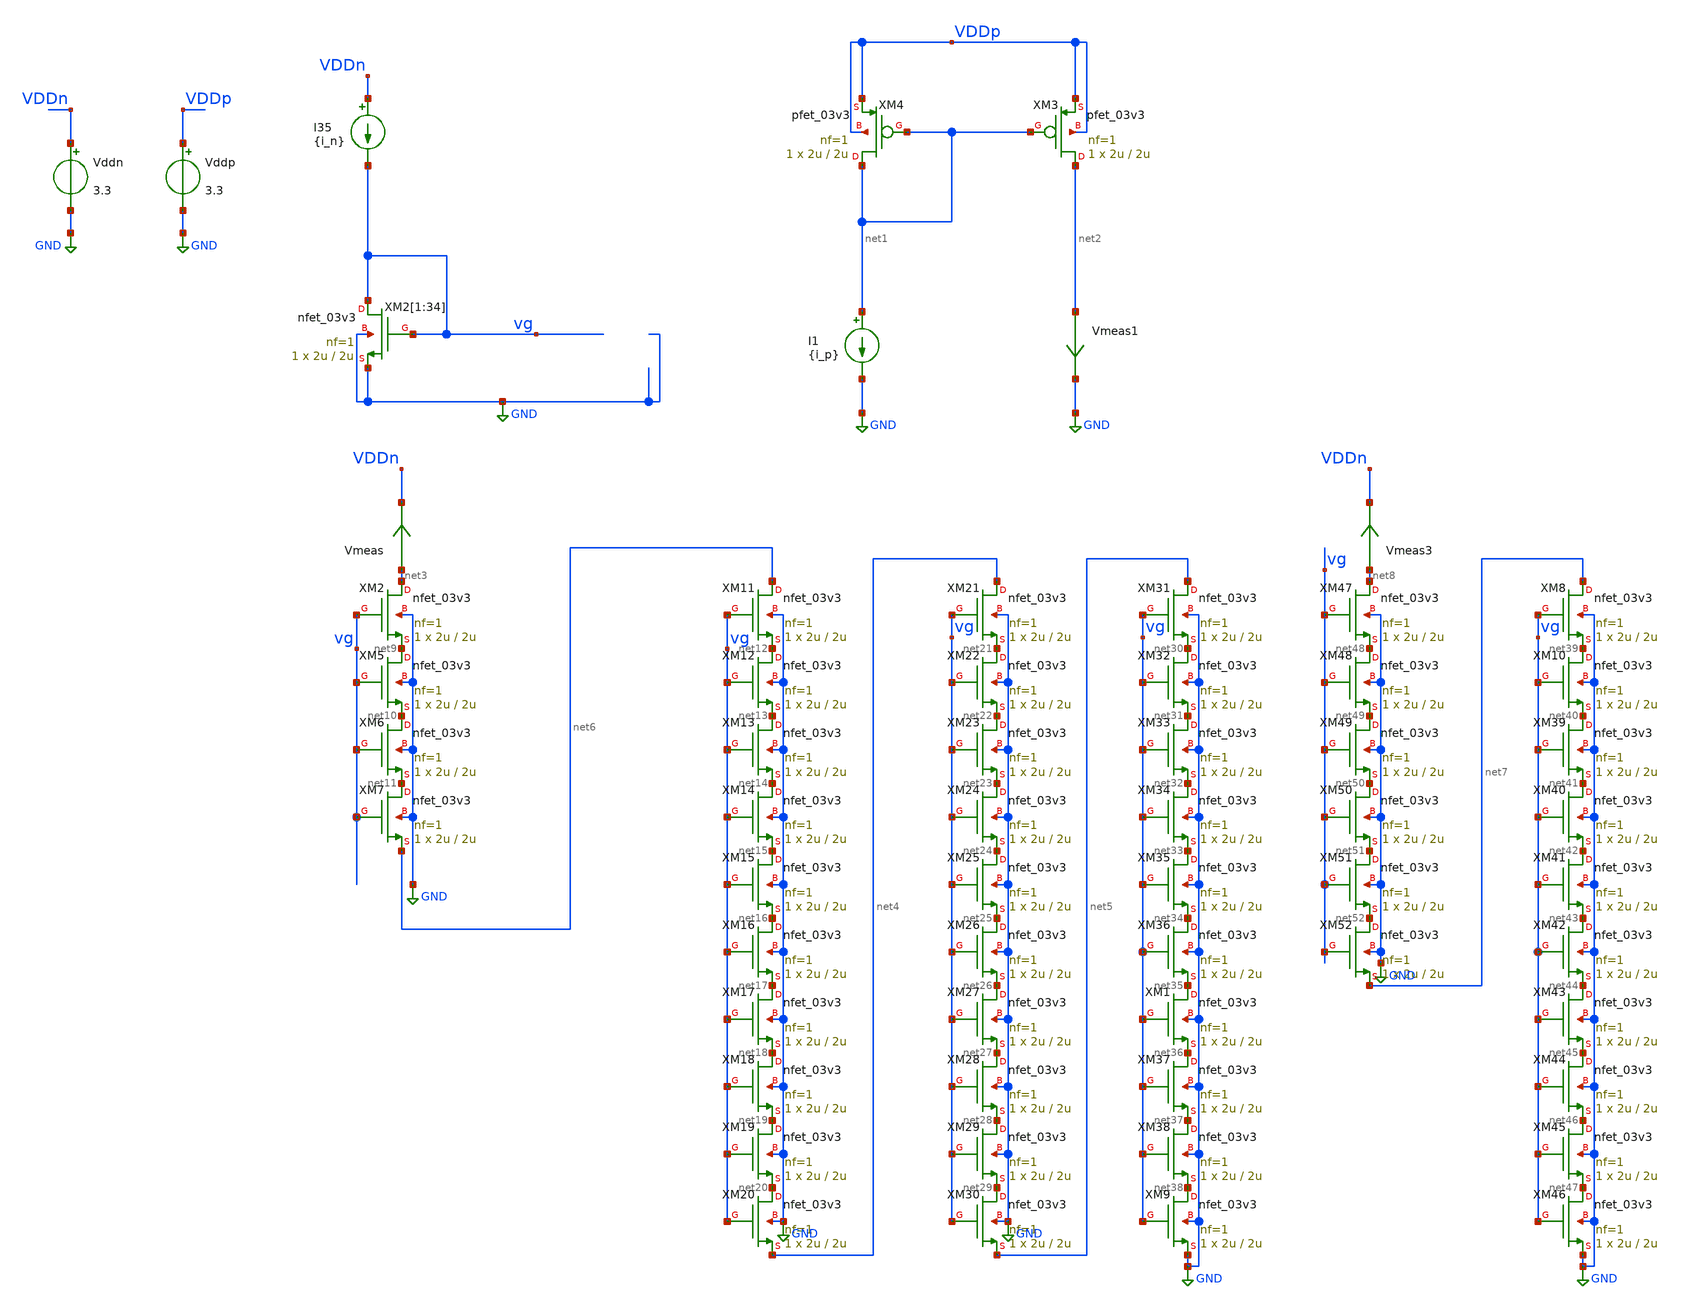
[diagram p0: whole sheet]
** sch_path: TIA_Filter/CurrentMirrors/TB_CM.sch
**.subckt TB_CM
XM2[1] vg vg GND GND nfet_03v3 L=2u W=2u nf=1 ad='int((nf+1)/2) * W/nf * 0.18u' as='int((nf+2)/2) * W/nf * 0.18u'
+ pd='2*int((nf+1)/2) * (W/nf + 0.18u)' ps='2*int((nf+2)/2) * (W/nf + 0.18u)' nrd='0.18u / W' nrs='0.18u / W'
+ sa=0 sb=0 sd=0 m=1
XM2[2] vg vg GND GND nfet_03v3 L=2u W=2u nf=1 ad='int((nf+1)/2) * W/nf * 0.18u' as='int((nf+2)/2) * W/nf * 0.18u'
+ pd='2*int((nf+1)/2) * (W/nf + 0.18u)' ps='2*int((nf+2)/2) * (W/nf + 0.18u)' nrd='0.18u / W' nrs='0.18u / W'
+ sa=0 sb=0 sd=0 m=1
XM2[3] vg vg GND GND nfet_03v3 L=2u W=2u nf=1 ad='int((nf+1)/2) * W/nf * 0.18u' as='int((nf+2)/2) * W/nf * 0.18u'
+ pd='2*int((nf+1)/2) * (W/nf + 0.18u)' ps='2*int((nf+2)/2) * (W/nf + 0.18u)' nrd='0.18u / W' nrs='0.18u / W'
+ sa=0 sb=0 sd=0 m=1
XM2[4] vg vg GND GND nfet_03v3 L=2u W=2u nf=1 ad='int((nf+1)/2) * W/nf * 0.18u' as='int((nf+2)/2) * W/nf * 0.18u'
+ pd='2*int((nf+1)/2) * (W/nf + 0.18u)' ps='2*int((nf+2)/2) * (W/nf + 0.18u)' nrd='0.18u / W' nrs='0.18u / W'
+ sa=0 sb=0 sd=0 m=1
XM2[5] vg vg GND GND nfet_03v3 L=2u W=2u nf=1 ad='int((nf+1)/2) * W/nf * 0.18u' as='int((nf+2)/2) * W/nf * 0.18u'
+ pd='2*int((nf+1)/2) * (W/nf + 0.18u)' ps='2*int((nf+2)/2) * (W/nf + 0.18u)' nrd='0.18u / W' nrs='0.18u / W'
+ sa=0 sb=0 sd=0 m=1
XM2[6] vg vg GND GND nfet_03v3 L=2u W=2u nf=1 ad='int((nf+1)/2) * W/nf * 0.18u' as='int((nf+2)/2) * W/nf * 0.18u'
+ pd='2*int((nf+1)/2) * (W/nf + 0.18u)' ps='2*int((nf+2)/2) * (W/nf + 0.18u)' nrd='0.18u / W' nrs='0.18u / W'
+ sa=0 sb=0 sd=0 m=1
XM2[7] vg vg GND GND nfet_03v3 L=2u W=2u nf=1 ad='int((nf+1)/2) * W/nf * 0.18u' as='int((nf+2)/2) * W/nf * 0.18u'
+ pd='2*int((nf+1)/2) * (W/nf + 0.18u)' ps='2*int((nf+2)/2) * (W/nf + 0.18u)' nrd='0.18u / W' nrs='0.18u / W'
+ sa=0 sb=0 sd=0 m=1
XM2[8] vg vg GND GND nfet_03v3 L=2u W=2u nf=1 ad='int((nf+1)/2) * W/nf * 0.18u' as='int((nf+2)/2) * W/nf * 0.18u'
+ pd='2*int((nf+1)/2) * (W/nf + 0.18u)' ps='2*int((nf+2)/2) * (W/nf + 0.18u)' nrd='0.18u / W' nrs='0.18u / W'
+ sa=0 sb=0 sd=0 m=1
XM2[9] vg vg GND GND nfet_03v3 L=2u W=2u nf=1 ad='int((nf+1)/2) * W/nf * 0.18u' as='int((nf+2)/2) * W/nf * 0.18u'
+ pd='2*int((nf+1)/2) * (W/nf + 0.18u)' ps='2*int((nf+2)/2) * (W/nf + 0.18u)' nrd='0.18u / W' nrs='0.18u / W'
+ sa=0 sb=0 sd=0 m=1
XM2[10] vg vg GND GND nfet_03v3 L=2u W=2u nf=1 ad='int((nf+1)/2) * W/nf * 0.18u' as='int((nf+2)/2) * W/nf * 0.18u'
+ pd='2*int((nf+1)/2) * (W/nf + 0.18u)' ps='2*int((nf+2)/2) * (W/nf + 0.18u)' nrd='0.18u / W' nrs='0.18u / W'
+ sa=0 sb=0 sd=0 m=1
XM2[11] vg vg GND GND nfet_03v3 L=2u W=2u nf=1 ad='int((nf+1)/2) * W/nf * 0.18u' as='int((nf+2)/2) * W/nf * 0.18u'
+ pd='2*int((nf+1)/2) * (W/nf + 0.18u)' ps='2*int((nf+2)/2) * (W/nf + 0.18u)' nrd='0.18u / W' nrs='0.18u / W'
+ sa=0 sb=0 sd=0 m=1
XM2[12] vg vg GND GND nfet_03v3 L=2u W=2u nf=1 ad='int((nf+1)/2) * W/nf * 0.18u' as='int((nf+2)/2) * W/nf * 0.18u'
+ pd='2*int((nf+1)/2) * (W/nf + 0.18u)' ps='2*int((nf+2)/2) * (W/nf + 0.18u)' nrd='0.18u / W' nrs='0.18u / W'
+ sa=0 sb=0 sd=0 m=1
XM2[13] vg vg GND GND nfet_03v3 L=2u W=2u nf=1 ad='int((nf+1)/2) * W/nf * 0.18u' as='int((nf+2)/2) * W/nf * 0.18u'
+ pd='2*int((nf+1)/2) * (W/nf + 0.18u)' ps='2*int((nf+2)/2) * (W/nf + 0.18u)' nrd='0.18u / W' nrs='0.18u / W'
+ sa=0 sb=0 sd=0 m=1
XM2[14] vg vg GND GND nfet_03v3 L=2u W=2u nf=1 ad='int((nf+1)/2) * W/nf * 0.18u' as='int((nf+2)/2) * W/nf * 0.18u'
+ pd='2*int((nf+1)/2) * (W/nf + 0.18u)' ps='2*int((nf+2)/2) * (W/nf + 0.18u)' nrd='0.18u / W' nrs='0.18u / W'
+ sa=0 sb=0 sd=0 m=1
XM2[15] vg vg GND GND nfet_03v3 L=2u W=2u nf=1 ad='int((nf+1)/2) * W/nf * 0.18u' as='int((nf+2)/2) * W/nf * 0.18u'
+ pd='2*int((nf+1)/2) * (W/nf + 0.18u)' ps='2*int((nf+2)/2) * (W/nf + 0.18u)' nrd='0.18u / W' nrs='0.18u / W'
+ sa=0 sb=0 sd=0 m=1
XM2[16] vg vg GND GND nfet_03v3 L=2u W=2u nf=1 ad='int((nf+1)/2) * W/nf * 0.18u' as='int((nf+2)/2) * W/nf * 0.18u'
+ pd='2*int((nf+1)/2) * (W/nf + 0.18u)' ps='2*int((nf+2)/2) * (W/nf + 0.18u)' nrd='0.18u / W' nrs='0.18u / W'
+ sa=0 sb=0 sd=0 m=1
XM2[17] vg vg GND GND nfet_03v3 L=2u W=2u nf=1 ad='int((nf+1)/2) * W/nf * 0.18u' as='int((nf+2)/2) * W/nf * 0.18u'
+ pd='2*int((nf+1)/2) * (W/nf + 0.18u)' ps='2*int((nf+2)/2) * (W/nf + 0.18u)' nrd='0.18u / W' nrs='0.18u / W'
+ sa=0 sb=0 sd=0 m=1
XM2[18] vg vg GND GND nfet_03v3 L=2u W=2u nf=1 ad='int((nf+1)/2) * W/nf * 0.18u' as='int((nf+2)/2) * W/nf * 0.18u'
+ pd='2*int((nf+1)/2) * (W/nf + 0.18u)' ps='2*int((nf+2)/2) * (W/nf + 0.18u)' nrd='0.18u / W' nrs='0.18u / W'
+ sa=0 sb=0 sd=0 m=1
XM2[19] vg vg GND GND nfet_03v3 L=2u W=2u nf=1 ad='int((nf+1)/2) * W/nf * 0.18u' as='int((nf+2)/2) * W/nf * 0.18u'
+ pd='2*int((nf+1)/2) * (W/nf + 0.18u)' ps='2*int((nf+2)/2) * (W/nf + 0.18u)' nrd='0.18u / W' nrs='0.18u / W'
+ sa=0 sb=0 sd=0 m=1
XM2[20] vg vg GND GND nfet_03v3 L=2u W=2u nf=1 ad='int((nf+1)/2) * W/nf * 0.18u' as='int((nf+2)/2) * W/nf * 0.18u'
+ pd='2*int((nf+1)/2) * (W/nf + 0.18u)' ps='2*int((nf+2)/2) * (W/nf + 0.18u)' nrd='0.18u / W' nrs='0.18u / W'
+ sa=0 sb=0 sd=0 m=1
XM2[21] vg vg GND GND nfet_03v3 L=2u W=2u nf=1 ad='int((nf+1)/2) * W/nf * 0.18u' as='int((nf+2)/2) * W/nf * 0.18u'
+ pd='2*int((nf+1)/2) * (W/nf + 0.18u)' ps='2*int((nf+2)/2) * (W/nf + 0.18u)' nrd='0.18u / W' nrs='0.18u / W'
+ sa=0 sb=0 sd=0 m=1
XM2[22] vg vg GND GND nfet_03v3 L=2u W=2u nf=1 ad='int((nf+1)/2) * W/nf * 0.18u' as='int((nf+2)/2) * W/nf * 0.18u'
+ pd='2*int((nf+1)/2) * (W/nf + 0.18u)' ps='2*int((nf+2)/2) * (W/nf + 0.18u)' nrd='0.18u / W' nrs='0.18u / W'
+ sa=0 sb=0 sd=0 m=1
XM2[23] vg vg GND GND nfet_03v3 L=2u W=2u nf=1 ad='int((nf+1)/2) * W/nf * 0.18u' as='int((nf+2)/2) * W/nf * 0.18u'
+ pd='2*int((nf+1)/2) * (W/nf + 0.18u)' ps='2*int((nf+2)/2) * (W/nf + 0.18u)' nrd='0.18u / W' nrs='0.18u / W'
+ sa=0 sb=0 sd=0 m=1
XM2[24] vg vg GND GND nfet_03v3 L=2u W=2u nf=1 ad='int((nf+1)/2) * W/nf * 0.18u' as='int((nf+2)/2) * W/nf * 0.18u'
+ pd='2*int((nf+1)/2) * (W/nf + 0.18u)' ps='2*int((nf+2)/2) * (W/nf + 0.18u)' nrd='0.18u / W' nrs='0.18u / W'
+ sa=0 sb=0 sd=0 m=1
XM2[25] vg vg GND GND nfet_03v3 L=2u W=2u nf=1 ad='int((nf+1)/2) * W/nf * 0.18u' as='int((nf+2)/2) * W/nf * 0.18u'
+ pd='2*int((nf+1)/2) * (W/nf + 0.18u)' ps='2*int((nf+2)/2) * (W/nf + 0.18u)' nrd='0.18u / W' nrs='0.18u / W'
+ sa=0 sb=0 sd=0 m=1
XM2[26] vg vg GND GND nfet_03v3 L=2u W=2u nf=1 ad='int((nf+1)/2) * W/nf * 0.18u' as='int((nf+2)/2) * W/nf * 0.18u'
+ pd='2*int((nf+1)/2) * (W/nf + 0.18u)' ps='2*int((nf+2)/2) * (W/nf + 0.18u)' nrd='0.18u / W' nrs='0.18u / W'
+ sa=0 sb=0 sd=0 m=1
XM2[27] vg vg GND GND nfet_03v3 L=2u W=2u nf=1 ad='int((nf+1)/2) * W/nf * 0.18u' as='int((nf+2)/2) * W/nf * 0.18u'
+ pd='2*int((nf+1)/2) * (W/nf + 0.18u)' ps='2*int((nf+2)/2) * (W/nf + 0.18u)' nrd='0.18u / W' nrs='0.18u / W'
+ sa=0 sb=0 sd=0 m=1
XM2[28] vg vg GND GND nfet_03v3 L=2u W=2u nf=1 ad='int((nf+1)/2) * W/nf * 0.18u' as='int((nf+2)/2) * W/nf * 0.18u'
+ pd='2*int((nf+1)/2) * (W/nf + 0.18u)' ps='2*int((nf+2)/2) * (W/nf + 0.18u)' nrd='0.18u / W' nrs='0.18u / W'
+ sa=0 sb=0 sd=0 m=1
XM2[29] vg vg GND GND nfet_03v3 L=2u W=2u nf=1 ad='int((nf+1)/2) * W/nf * 0.18u' as='int((nf+2)/2) * W/nf * 0.18u'
+ pd='2*int((nf+1)/2) * (W/nf + 0.18u)' ps='2*int((nf+2)/2) * (W/nf + 0.18u)' nrd='0.18u / W' nrs='0.18u / W'
+ sa=0 sb=0 sd=0 m=1
XM2[30] vg vg GND GND nfet_03v3 L=2u W=2u nf=1 ad='int((nf+1)/2) * W/nf * 0.18u' as='int((nf+2)/2) * W/nf * 0.18u'
+ pd='2*int((nf+1)/2) * (W/nf + 0.18u)' ps='2*int((nf+2)/2) * (W/nf + 0.18u)' nrd='0.18u / W' nrs='0.18u / W'
+ sa=0 sb=0 sd=0 m=1
XM2[31] vg vg GND GND nfet_03v3 L=2u W=2u nf=1 ad='int((nf+1)/2) * W/nf * 0.18u' as='int((nf+2)/2) * W/nf * 0.18u'
+ pd='2*int((nf+1)/2) * (W/nf + 0.18u)' ps='2*int((nf+2)/2) * (W/nf + 0.18u)' nrd='0.18u / W' nrs='0.18u / W'
+ sa=0 sb=0 sd=0 m=1
XM2[32] vg vg GND GND nfet_03v3 L=2u W=2u nf=1 ad='int((nf+1)/2) * W/nf * 0.18u' as='int((nf+2)/2) * W/nf * 0.18u'
+ pd='2*int((nf+1)/2) * (W/nf + 0.18u)' ps='2*int((nf+2)/2) * (W/nf + 0.18u)' nrd='0.18u / W' nrs='0.18u / W'
+ sa=0 sb=0 sd=0 m=1
XM2[33] vg vg GND GND nfet_03v3 L=2u W=2u nf=1 ad='int((nf+1)/2) * W/nf * 0.18u' as='int((nf+2)/2) * W/nf * 0.18u'
+ pd='2*int((nf+1)/2) * (W/nf + 0.18u)' ps='2*int((nf+2)/2) * (W/nf + 0.18u)' nrd='0.18u / W' nrs='0.18u / W'
+ sa=0 sb=0 sd=0 m=1
XM2[34] vg vg GND GND nfet_03v3 L=2u W=2u nf=1 ad='int((nf+1)/2) * W/nf * 0.18u' as='int((nf+2)/2) * W/nf * 0.18u'
+ pd='2*int((nf+1)/2) * (W/nf + 0.18u)' ps='2*int((nf+2)/2) * (W/nf + 0.18u)' nrd='0.18u / W' nrs='0.18u / W'
+ sa=0 sb=0 sd=0 m=1
XM3 net2 net1 VDDp VDDp pfet_03v3 L=2u W=2u nf=1 ad='int((nf+1)/2) * W/nf * 0.18u' as='int((nf+2)/2) * W/nf * 0.18u'
+ pd='2*int((nf+1)/2) * (W/nf + 0.18u)' ps='2*int((nf+2)/2) * (W/nf + 0.18u)' nrd='0.18u / W' nrs='0.18u / W'
+ sa=0 sb=0 sd=0 m=1
XM4 net1 net1 VDDp VDDp pfet_03v3 L=2u W=2u nf=1 ad='int((nf+1)/2) * W/nf * 0.18u' as='int((nf+2)/2) * W/nf * 0.18u'
+ pd='2*int((nf+1)/2) * (W/nf + 0.18u)' ps='2*int((nf+2)/2) * (W/nf + 0.18u)' nrd='0.18u / W' nrs='0.18u / W'
+ sa=0 sb=0 sd=0 m=1
I35 VDDn vg {i_n}
I1 net1 GND {i_p}
Vddn VDDn GND 3.3
Vddp VDDp GND 3.3
Vmeas net3 VDDn 0
.save i(vmeas)
Vmeas1 net2 GND 0
.save i(vmeas1)
XM2 net3 vg net9 GND nfet_03v3 L=2u W=2u nf=1 ad='int((nf+1)/2) * W/nf * 0.18u' as='int((nf+2)/2) * W/nf * 0.18u'
+ pd='2*int((nf+1)/2) * (W/nf + 0.18u)' ps='2*int((nf+2)/2) * (W/nf + 0.18u)' nrd='0.18u / W' nrs='0.18u / W'
+ sa=0 sb=0 sd=0 m=1
XM5 net9 vg net10 GND nfet_03v3 L=2u W=2u nf=1 ad='int((nf+1)/2) * W/nf * 0.18u' as='int((nf+2)/2) * W/nf * 0.18u'
+ pd='2*int((nf+1)/2) * (W/nf + 0.18u)' ps='2*int((nf+2)/2) * (W/nf + 0.18u)' nrd='0.18u / W' nrs='0.18u / W'
+ sa=0 sb=0 sd=0 m=1
XM6 net10 vg net11 GND nfet_03v3 L=2u W=2u nf=1 ad='int((nf+1)/2) * W/nf * 0.18u' as='int((nf+2)/2) * W/nf * 0.18u'
+ pd='2*int((nf+1)/2) * (W/nf + 0.18u)' ps='2*int((nf+2)/2) * (W/nf + 0.18u)' nrd='0.18u / W' nrs='0.18u / W'
+ sa=0 sb=0 sd=0 m=1
XM7 net11 vg net6 GND nfet_03v3 L=2u W=2u nf=1 ad='int((nf+1)/2) * W/nf * 0.18u' as='int((nf+2)/2) * W/nf * 0.18u'
+ pd='2*int((nf+1)/2) * (W/nf + 0.18u)' ps='2*int((nf+2)/2) * (W/nf + 0.18u)' nrd='0.18u / W' nrs='0.18u / W'
+ sa=0 sb=0 sd=0 m=1
XM11 net6 vg net12 GND nfet_03v3 L=2u W=2u nf=1 ad='int((nf+1)/2) * W/nf * 0.18u' as='int((nf+2)/2) * W/nf * 0.18u'
+ pd='2*int((nf+1)/2) * (W/nf + 0.18u)' ps='2*int((nf+2)/2) * (W/nf + 0.18u)' nrd='0.18u / W' nrs='0.18u / W'
+ sa=0 sb=0 sd=0 m=1
XM12 net12 vg net13 GND nfet_03v3 L=2u W=2u nf=1 ad='int((nf+1)/2) * W/nf * 0.18u' as='int((nf+2)/2) * W/nf * 0.18u'
+ pd='2*int((nf+1)/2) * (W/nf + 0.18u)' ps='2*int((nf+2)/2) * (W/nf + 0.18u)' nrd='0.18u / W' nrs='0.18u / W'
+ sa=0 sb=0 sd=0 m=1
XM13 net13 vg net14 GND nfet_03v3 L=2u W=2u nf=1 ad='int((nf+1)/2) * W/nf * 0.18u' as='int((nf+2)/2) * W/nf * 0.18u'
+ pd='2*int((nf+1)/2) * (W/nf + 0.18u)' ps='2*int((nf+2)/2) * (W/nf + 0.18u)' nrd='0.18u / W' nrs='0.18u / W'
+ sa=0 sb=0 sd=0 m=1
XM14 net14 vg net15 GND nfet_03v3 L=2u W=2u nf=1 ad='int((nf+1)/2) * W/nf * 0.18u' as='int((nf+2)/2) * W/nf * 0.18u'
+ pd='2*int((nf+1)/2) * (W/nf + 0.18u)' ps='2*int((nf+2)/2) * (W/nf + 0.18u)' nrd='0.18u / W' nrs='0.18u / W'
+ sa=0 sb=0 sd=0 m=1
XM15 net15 vg net16 GND nfet_03v3 L=2u W=2u nf=1 ad='int((nf+1)/2) * W/nf * 0.18u' as='int((nf+2)/2) * W/nf * 0.18u'
+ pd='2*int((nf+1)/2) * (W/nf + 0.18u)' ps='2*int((nf+2)/2) * (W/nf + 0.18u)' nrd='0.18u / W' nrs='0.18u / W'
+ sa=0 sb=0 sd=0 m=1
XM16 net16 vg net17 GND nfet_03v3 L=2u W=2u nf=1 ad='int((nf+1)/2) * W/nf * 0.18u' as='int((nf+2)/2) * W/nf * 0.18u'
+ pd='2*int((nf+1)/2) * (W/nf + 0.18u)' ps='2*int((nf+2)/2) * (W/nf + 0.18u)' nrd='0.18u / W' nrs='0.18u / W'
+ sa=0 sb=0 sd=0 m=1
XM17 net17 vg net18 GND nfet_03v3 L=2u W=2u nf=1 ad='int((nf+1)/2) * W/nf * 0.18u' as='int((nf+2)/2) * W/nf * 0.18u'
+ pd='2*int((nf+1)/2) * (W/nf + 0.18u)' ps='2*int((nf+2)/2) * (W/nf + 0.18u)' nrd='0.18u / W' nrs='0.18u / W'
+ sa=0 sb=0 sd=0 m=1
XM18 net18 vg net19 GND nfet_03v3 L=2u W=2u nf=1 ad='int((nf+1)/2) * W/nf * 0.18u' as='int((nf+2)/2) * W/nf * 0.18u'
+ pd='2*int((nf+1)/2) * (W/nf + 0.18u)' ps='2*int((nf+2)/2) * (W/nf + 0.18u)' nrd='0.18u / W' nrs='0.18u / W'
+ sa=0 sb=0 sd=0 m=1
XM19 net19 vg net20 GND nfet_03v3 L=2u W=2u nf=1 ad='int((nf+1)/2) * W/nf * 0.18u' as='int((nf+2)/2) * W/nf * 0.18u'
+ pd='2*int((nf+1)/2) * (W/nf + 0.18u)' ps='2*int((nf+2)/2) * (W/nf + 0.18u)' nrd='0.18u / W' nrs='0.18u / W'
+ sa=0 sb=0 sd=0 m=1
XM20 net20 vg net4 GND nfet_03v3 L=2u W=2u nf=1 ad='int((nf+1)/2) * W/nf * 0.18u' as='int((nf+2)/2) * W/nf * 0.18u'
+ pd='2*int((nf+1)/2) * (W/nf + 0.18u)' ps='2*int((nf+2)/2) * (W/nf + 0.18u)' nrd='0.18u / W' nrs='0.18u / W'
+ sa=0 sb=0 sd=0 m=1
XM21 net4 vg net21 GND nfet_03v3 L=2u W=2u nf=1 ad='int((nf+1)/2) * W/nf * 0.18u' as='int((nf+2)/2) * W/nf * 0.18u'
+ pd='2*int((nf+1)/2) * (W/nf + 0.18u)' ps='2*int((nf+2)/2) * (W/nf + 0.18u)' nrd='0.18u / W' nrs='0.18u / W'
+ sa=0 sb=0 sd=0 m=1
XM22 net21 vg net22 GND nfet_03v3 L=2u W=2u nf=1 ad='int((nf+1)/2) * W/nf * 0.18u' as='int((nf+2)/2) * W/nf * 0.18u'
+ pd='2*int((nf+1)/2) * (W/nf + 0.18u)' ps='2*int((nf+2)/2) * (W/nf + 0.18u)' nrd='0.18u / W' nrs='0.18u / W'
+ sa=0 sb=0 sd=0 m=1
XM23 net22 vg net23 GND nfet_03v3 L=2u W=2u nf=1 ad='int((nf+1)/2) * W/nf * 0.18u' as='int((nf+2)/2) * W/nf * 0.18u'
+ pd='2*int((nf+1)/2) * (W/nf + 0.18u)' ps='2*int((nf+2)/2) * (W/nf + 0.18u)' nrd='0.18u / W' nrs='0.18u / W'
+ sa=0 sb=0 sd=0 m=1
XM24 net23 vg net24 GND nfet_03v3 L=2u W=2u nf=1 ad='int((nf+1)/2) * W/nf * 0.18u' as='int((nf+2)/2) * W/nf * 0.18u'
+ pd='2*int((nf+1)/2) * (W/nf + 0.18u)' ps='2*int((nf+2)/2) * (W/nf + 0.18u)' nrd='0.18u / W' nrs='0.18u / W'
+ sa=0 sb=0 sd=0 m=1
XM25 net24 vg net25 GND nfet_03v3 L=2u W=2u nf=1 ad='int((nf+1)/2) * W/nf * 0.18u' as='int((nf+2)/2) * W/nf * 0.18u'
+ pd='2*int((nf+1)/2) * (W/nf + 0.18u)' ps='2*int((nf+2)/2) * (W/nf + 0.18u)' nrd='0.18u / W' nrs='0.18u / W'
+ sa=0 sb=0 sd=0 m=1
XM26 net25 vg net26 GND nfet_03v3 L=2u W=2u nf=1 ad='int((nf+1)/2) * W/nf * 0.18u' as='int((nf+2)/2) * W/nf * 0.18u'
+ pd='2*int((nf+1)/2) * (W/nf + 0.18u)' ps='2*int((nf+2)/2) * (W/nf + 0.18u)' nrd='0.18u / W' nrs='0.18u / W'
+ sa=0 sb=0 sd=0 m=1
XM27 net26 vg net27 GND nfet_03v3 L=2u W=2u nf=1 ad='int((nf+1)/2) * W/nf * 0.18u' as='int((nf+2)/2) * W/nf * 0.18u'
+ pd='2*int((nf+1)/2) * (W/nf + 0.18u)' ps='2*int((nf+2)/2) * (W/nf + 0.18u)' nrd='0.18u / W' nrs='0.18u / W'
+ sa=0 sb=0 sd=0 m=1
XM28 net27 vg net28 GND nfet_03v3 L=2u W=2u nf=1 ad='int((nf+1)/2) * W/nf * 0.18u' as='int((nf+2)/2) * W/nf * 0.18u'
+ pd='2*int((nf+1)/2) * (W/nf + 0.18u)' ps='2*int((nf+2)/2) * (W/nf + 0.18u)' nrd='0.18u / W' nrs='0.18u / W'
+ sa=0 sb=0 sd=0 m=1
XM29 net28 vg net29 GND nfet_03v3 L=2u W=2u nf=1 ad='int((nf+1)/2) * W/nf * 0.18u' as='int((nf+2)/2) * W/nf * 0.18u'
+ pd='2*int((nf+1)/2) * (W/nf + 0.18u)' ps='2*int((nf+2)/2) * (W/nf + 0.18u)' nrd='0.18u / W' nrs='0.18u / W'
+ sa=0 sb=0 sd=0 m=1
XM30 net29 vg net5 GND nfet_03v3 L=2u W=2u nf=1 ad='int((nf+1)/2) * W/nf * 0.18u' as='int((nf+2)/2) * W/nf * 0.18u'
+ pd='2*int((nf+1)/2) * (W/nf + 0.18u)' ps='2*int((nf+2)/2) * (W/nf + 0.18u)' nrd='0.18u / W' nrs='0.18u / W'
+ sa=0 sb=0 sd=0 m=1
XM31 net5 vg net30 GND nfet_03v3 L=2u W=2u nf=1 ad='int((nf+1)/2) * W/nf * 0.18u' as='int((nf+2)/2) * W/nf * 0.18u'
+ pd='2*int((nf+1)/2) * (W/nf + 0.18u)' ps='2*int((nf+2)/2) * (W/nf + 0.18u)' nrd='0.18u / W' nrs='0.18u / W'
+ sa=0 sb=0 sd=0 m=1
XM32 net30 vg net31 GND nfet_03v3 L=2u W=2u nf=1 ad='int((nf+1)/2) * W/nf * 0.18u' as='int((nf+2)/2) * W/nf * 0.18u'
+ pd='2*int((nf+1)/2) * (W/nf + 0.18u)' ps='2*int((nf+2)/2) * (W/nf + 0.18u)' nrd='0.18u / W' nrs='0.18u / W'
+ sa=0 sb=0 sd=0 m=1
XM33 net31 vg net32 GND nfet_03v3 L=2u W=2u nf=1 ad='int((nf+1)/2) * W/nf * 0.18u' as='int((nf+2)/2) * W/nf * 0.18u'
+ pd='2*int((nf+1)/2) * (W/nf + 0.18u)' ps='2*int((nf+2)/2) * (W/nf + 0.18u)' nrd='0.18u / W' nrs='0.18u / W'
+ sa=0 sb=0 sd=0 m=1
XM34 net32 vg net33 GND nfet_03v3 L=2u W=2u nf=1 ad='int((nf+1)/2) * W/nf * 0.18u' as='int((nf+2)/2) * W/nf * 0.18u'
+ pd='2*int((nf+1)/2) * (W/nf + 0.18u)' ps='2*int((nf+2)/2) * (W/nf + 0.18u)' nrd='0.18u / W' nrs='0.18u / W'
+ sa=0 sb=0 sd=0 m=1
XM35 net33 vg net34 GND nfet_03v3 L=2u W=2u nf=1 ad='int((nf+1)/2) * W/nf * 0.18u' as='int((nf+2)/2) * W/nf * 0.18u'
+ pd='2*int((nf+1)/2) * (W/nf + 0.18u)' ps='2*int((nf+2)/2) * (W/nf + 0.18u)' nrd='0.18u / W' nrs='0.18u / W'
+ sa=0 sb=0 sd=0 m=1
XM36 net34 vg net35 GND nfet_03v3 L=2u W=2u nf=1 ad='int((nf+1)/2) * W/nf * 0.18u' as='int((nf+2)/2) * W/nf * 0.18u'
+ pd='2*int((nf+1)/2) * (W/nf + 0.18u)' ps='2*int((nf+2)/2) * (W/nf + 0.18u)' nrd='0.18u / W' nrs='0.18u / W'
+ sa=0 sb=0 sd=0 m=1
XM1 net35 vg net36 GND nfet_03v3 L=2u W=2u nf=1 ad='int((nf+1)/2) * W/nf * 0.18u' as='int((nf+2)/2) * W/nf * 0.18u'
+ pd='2*int((nf+1)/2) * (W/nf + 0.18u)' ps='2*int((nf+2)/2) * (W/nf + 0.18u)' nrd='0.18u / W' nrs='0.18u / W'
+ sa=0 sb=0 sd=0 m=1
XM37 net36 vg net37 GND nfet_03v3 L=2u W=2u nf=1 ad='int((nf+1)/2) * W/nf * 0.18u' as='int((nf+2)/2) * W/nf * 0.18u'
+ pd='2*int((nf+1)/2) * (W/nf + 0.18u)' ps='2*int((nf+2)/2) * (W/nf + 0.18u)' nrd='0.18u / W' nrs='0.18u / W'
+ sa=0 sb=0 sd=0 m=1
XM38 net37 vg net38 GND nfet_03v3 L=2u W=2u nf=1 ad='int((nf+1)/2) * W/nf * 0.18u' as='int((nf+2)/2) * W/nf * 0.18u'
+ pd='2*int((nf+1)/2) * (W/nf + 0.18u)' ps='2*int((nf+2)/2) * (W/nf + 0.18u)' nrd='0.18u / W' nrs='0.18u / W'
+ sa=0 sb=0 sd=0 m=1
XM9 net38 vg GND GND nfet_03v3 L=2u W=2u nf=1 ad='int((nf+1)/2) * W/nf * 0.18u' as='int((nf+2)/2) * W/nf * 0.18u'
+ pd='2*int((nf+1)/2) * (W/nf + 0.18u)' ps='2*int((nf+2)/2) * (W/nf + 0.18u)' nrd='0.18u / W' nrs='0.18u / W'
+ sa=0 sb=0 sd=0 m=1
XM8 net7 vg net39 GND nfet_03v3 L=2u W=2u nf=1 ad='int((nf+1)/2) * W/nf * 0.18u' as='int((nf+2)/2) * W/nf * 0.18u'
+ pd='2*int((nf+1)/2) * (W/nf + 0.18u)' ps='2*int((nf+2)/2) * (W/nf + 0.18u)' nrd='0.18u / W' nrs='0.18u / W'
+ sa=0 sb=0 sd=0 m=1
XM10 net39 vg net40 GND nfet_03v3 L=2u W=2u nf=1 ad='int((nf+1)/2) * W/nf * 0.18u' as='int((nf+2)/2) * W/nf * 0.18u'
+ pd='2*int((nf+1)/2) * (W/nf + 0.18u)' ps='2*int((nf+2)/2) * (W/nf + 0.18u)' nrd='0.18u / W' nrs='0.18u / W'
+ sa=0 sb=0 sd=0 m=1
XM39 net40 vg net41 GND nfet_03v3 L=2u W=2u nf=1 ad='int((nf+1)/2) * W/nf * 0.18u' as='int((nf+2)/2) * W/nf * 0.18u'
+ pd='2*int((nf+1)/2) * (W/nf + 0.18u)' ps='2*int((nf+2)/2) * (W/nf + 0.18u)' nrd='0.18u / W' nrs='0.18u / W'
+ sa=0 sb=0 sd=0 m=1
XM40 net41 vg net42 GND nfet_03v3 L=2u W=2u nf=1 ad='int((nf+1)/2) * W/nf * 0.18u' as='int((nf+2)/2) * W/nf * 0.18u'
+ pd='2*int((nf+1)/2) * (W/nf + 0.18u)' ps='2*int((nf+2)/2) * (W/nf + 0.18u)' nrd='0.18u / W' nrs='0.18u / W'
+ sa=0 sb=0 sd=0 m=1
XM41 net42 vg net43 GND nfet_03v3 L=2u W=2u nf=1 ad='int((nf+1)/2) * W/nf * 0.18u' as='int((nf+2)/2) * W/nf * 0.18u'
+ pd='2*int((nf+1)/2) * (W/nf + 0.18u)' ps='2*int((nf+2)/2) * (W/nf + 0.18u)' nrd='0.18u / W' nrs='0.18u / W'
+ sa=0 sb=0 sd=0 m=1
XM42 net43 vg net44 GND nfet_03v3 L=2u W=2u nf=1 ad='int((nf+1)/2) * W/nf * 0.18u' as='int((nf+2)/2) * W/nf * 0.18u'
+ pd='2*int((nf+1)/2) * (W/nf + 0.18u)' ps='2*int((nf+2)/2) * (W/nf + 0.18u)' nrd='0.18u / W' nrs='0.18u / W'
+ sa=0 sb=0 sd=0 m=1
XM43 net44 vg net45 GND nfet_03v3 L=2u W=2u nf=1 ad='int((nf+1)/2) * W/nf * 0.18u' as='int((nf+2)/2) * W/nf * 0.18u'
+ pd='2*int((nf+1)/2) * (W/nf + 0.18u)' ps='2*int((nf+2)/2) * (W/nf + 0.18u)' nrd='0.18u / W' nrs='0.18u / W'
+ sa=0 sb=0 sd=0 m=1
XM44 net45 vg net46 GND nfet_03v3 L=2u W=2u nf=1 ad='int((nf+1)/2) * W/nf * 0.18u' as='int((nf+2)/2) * W/nf * 0.18u'
+ pd='2*int((nf+1)/2) * (W/nf + 0.18u)' ps='2*int((nf+2)/2) * (W/nf + 0.18u)' nrd='0.18u / W' nrs='0.18u / W'
+ sa=0 sb=0 sd=0 m=1
XM45 net46 vg net47 GND nfet_03v3 L=2u W=2u nf=1 ad='int((nf+1)/2) * W/nf * 0.18u' as='int((nf+2)/2) * W/nf * 0.18u'
+ pd='2*int((nf+1)/2) * (W/nf + 0.18u)' ps='2*int((nf+2)/2) * (W/nf + 0.18u)' nrd='0.18u / W' nrs='0.18u / W'
+ sa=0 sb=0 sd=0 m=1
XM46 net47 vg GND GND nfet_03v3 L=2u W=2u nf=1 ad='int((nf+1)/2) * W/nf * 0.18u' as='int((nf+2)/2) * W/nf * 0.18u'
+ pd='2*int((nf+1)/2) * (W/nf + 0.18u)' ps='2*int((nf+2)/2) * (W/nf + 0.18u)' nrd='0.18u / W' nrs='0.18u / W'
+ sa=0 sb=0 sd=0 m=1
XM47 net8 vg net48 GND nfet_03v3 L=2u W=2u nf=1 ad='int((nf+1)/2) * W/nf * 0.18u' as='int((nf+2)/2) * W/nf * 0.18u'
+ pd='2*int((nf+1)/2) * (W/nf + 0.18u)' ps='2*int((nf+2)/2) * (W/nf + 0.18u)' nrd='0.18u / W' nrs='0.18u / W'
+ sa=0 sb=0 sd=0 m=1
XM48 net48 vg net49 GND nfet_03v3 L=2u W=2u nf=1 ad='int((nf+1)/2) * W/nf * 0.18u' as='int((nf+2)/2) * W/nf * 0.18u'
+ pd='2*int((nf+1)/2) * (W/nf + 0.18u)' ps='2*int((nf+2)/2) * (W/nf + 0.18u)' nrd='0.18u / W' nrs='0.18u / W'
+ sa=0 sb=0 sd=0 m=1
XM49 net49 vg net50 GND nfet_03v3 L=2u W=2u nf=1 ad='int((nf+1)/2) * W/nf * 0.18u' as='int((nf+2)/2) * W/nf * 0.18u'
+ pd='2*int((nf+1)/2) * (W/nf + 0.18u)' ps='2*int((nf+2)/2) * (W/nf + 0.18u)' nrd='0.18u / W' nrs='0.18u / W'
+ sa=0 sb=0 sd=0 m=1
XM50 net50 vg net51 GND nfet_03v3 L=2u W=2u nf=1 ad='int((nf+1)/2) * W/nf * 0.18u' as='int((nf+2)/2) * W/nf * 0.18u'
+ pd='2*int((nf+1)/2) * (W/nf + 0.18u)' ps='2*int((nf+2)/2) * (W/nf + 0.18u)' nrd='0.18u / W' nrs='0.18u / W'
+ sa=0 sb=0 sd=0 m=1
XM51 net51 vg net52 GND nfet_03v3 L=2u W=2u nf=1 ad='int((nf+1)/2) * W/nf * 0.18u' as='int((nf+2)/2) * W/nf * 0.18u'
+ pd='2*int((nf+1)/2) * (W/nf + 0.18u)' ps='2*int((nf+2)/2) * (W/nf + 0.18u)' nrd='0.18u / W' nrs='0.18u / W'
+ sa=0 sb=0 sd=0 m=1
XM52 net52 vg net7 GND nfet_03v3 L=2u W=2u nf=1 ad='int((nf+1)/2) * W/nf * 0.18u' as='int((nf+2)/2) * W/nf * 0.18u'
+ pd='2*int((nf+1)/2) * (W/nf + 0.18u)' ps='2*int((nf+2)/2) * (W/nf + 0.18u)' nrd='0.18u / W' nrs='0.18u / W'
+ sa=0 sb=0 sd=0 m=1
Vmeas3 net8 VDDn 0
.save i(vmeas3)
**** begin user architecture code

.include $::180MCU_MODELS/design.ngspice
.lib $::180MCU_MODELS/sm141064.ngspice typical
.param sw_stat_mismatch=1
.param sw_stat_global=1



.option gmin=1e-18
.param i_n=1n
.param i_p=1n

.control
save all

let sample_num = 0

while sample_num<151

reset
op
remzerovec
write TB_CM.raw
wrdata /home/gmaranhao/Desktop/Bracolin/TIA_Filter/CurrentMirrors/out_cm.txt i(Vmeas) i(Vmeas3)
set appendwrite

let sample_num = sample_num + 1
end


.endc
.save all


**** end user architecture code
**.ends
.GLOBAL GND
.end
